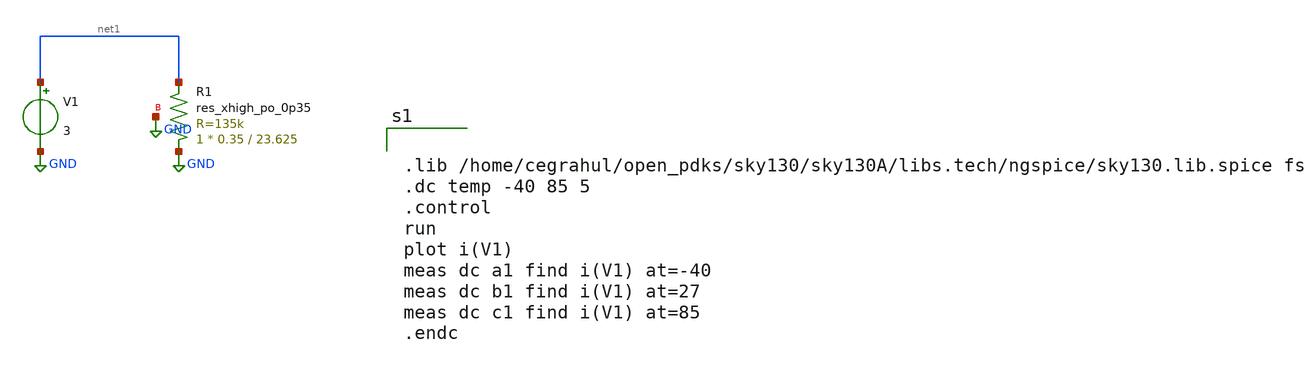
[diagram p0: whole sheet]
** sch_path: Polyres.sch
**.subckt Polyres
V1 net1 GND 3
XR1 GND net1 GND sky130_fd_pr__res_xhigh_po_0p35 L=23.625 mult=1 m=1
**** begin user architecture code


.lib /home/cegrahul/open_pdks/sky130/sky130A/libs.tech/ngspice/sky130.lib.spice fs
.dc temp -40 85 5
.control
run
plot i(V1)
meas dc a1 find i(V1) at=-40
meas dc b1 find i(V1) at=27
meas dc c1 find i(V1) at=85
.endc

**** end user architecture code
**.ends
.GLOBAL GND
.end
